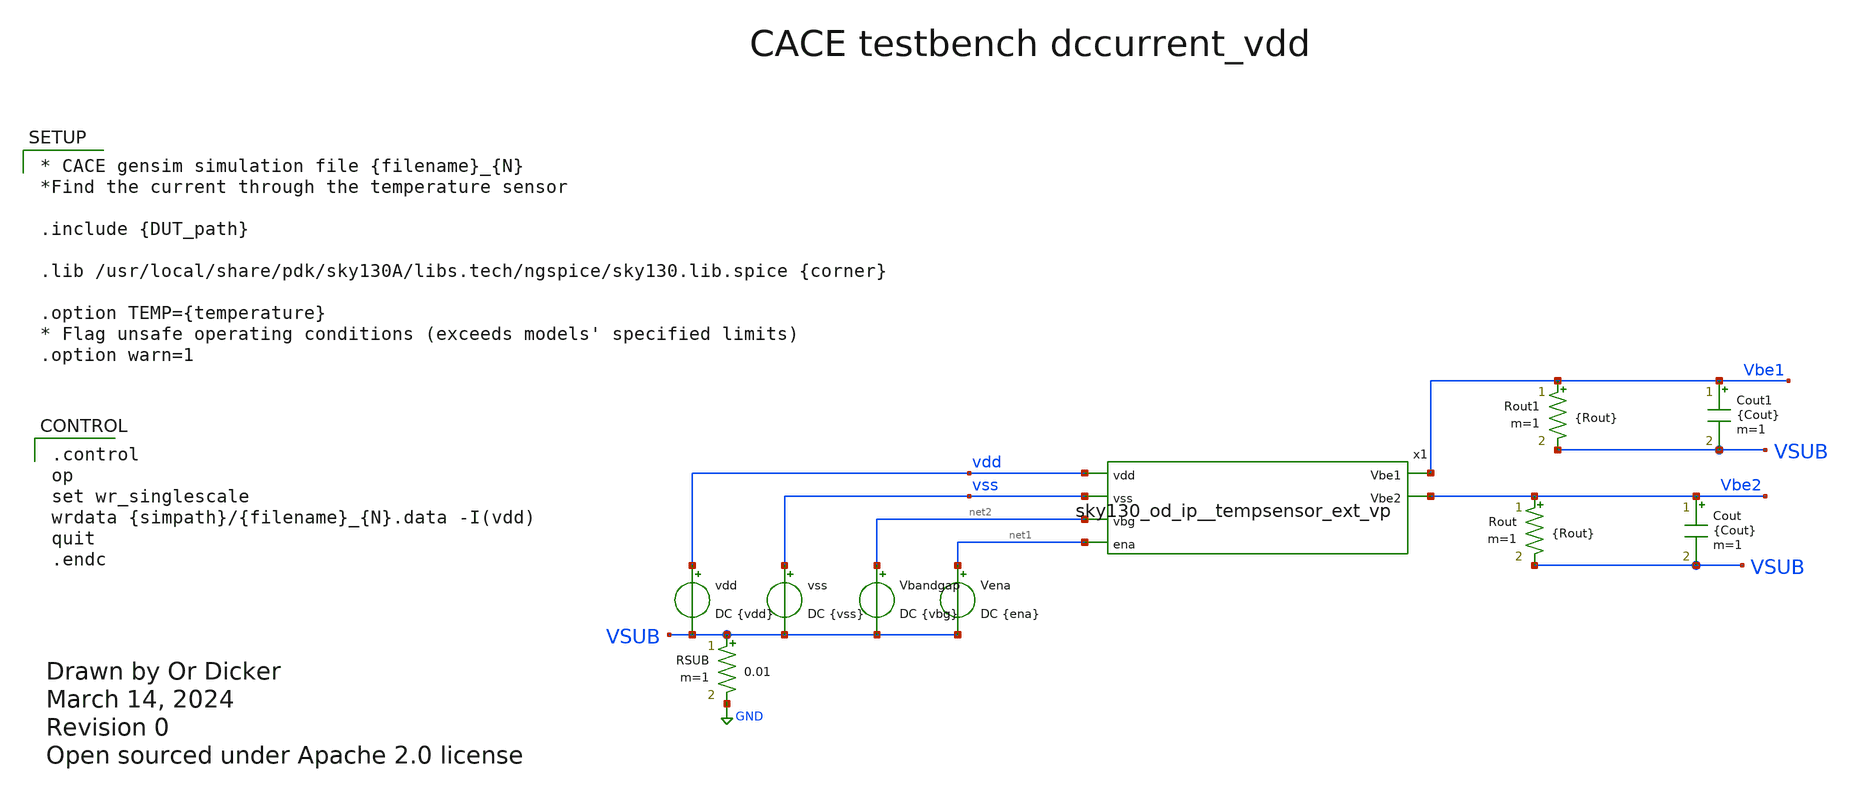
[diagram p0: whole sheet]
** sch_path: cace/templates/dccurrent_vdd.sch
* Open sourced under Apache 2.0 license
**.subckt dccurrent_vdd
vss vss VSUB DC {vss}
Rout Vbe2 VSUB {Rout} m=1
Cout Vbe2 VSUB {Cout} m=1
vdd vdd VSUB DC {vdd}
RSUB VSUB GND 0.01 m=1
Rout1 Vbe1 VSUB {Rout} m=1
Cout1 Vbe1 VSUB {Cout} m=1
Vena net1 VSUB DC {ena}
x1 vdd vss net2 Vbe1 Vbe2 net1 sky130_od_ip__tempsensor_ext_vp
Vbandgap net2 VSUB DC {vbg}
**** begin user architecture code

.control
op
set wr_singlescale
wrdata {simpath}/{filename}_{N}.data -I(vdd)
quit
.endc



* CACE gensim simulation file {filename}_{N}
*Find the current through the temperature sensor

.include {DUT_path}

.lib /usr/local/share/pdk/sky130A/libs.tech/ngspice/sky130.lib.spice {corner}

.option TEMP={temperature}
* Flag unsafe operating conditions (exceeds models' specified limits)
.option warn=1


**** end user architecture code
**.ends
.GLOBAL GND
.end
